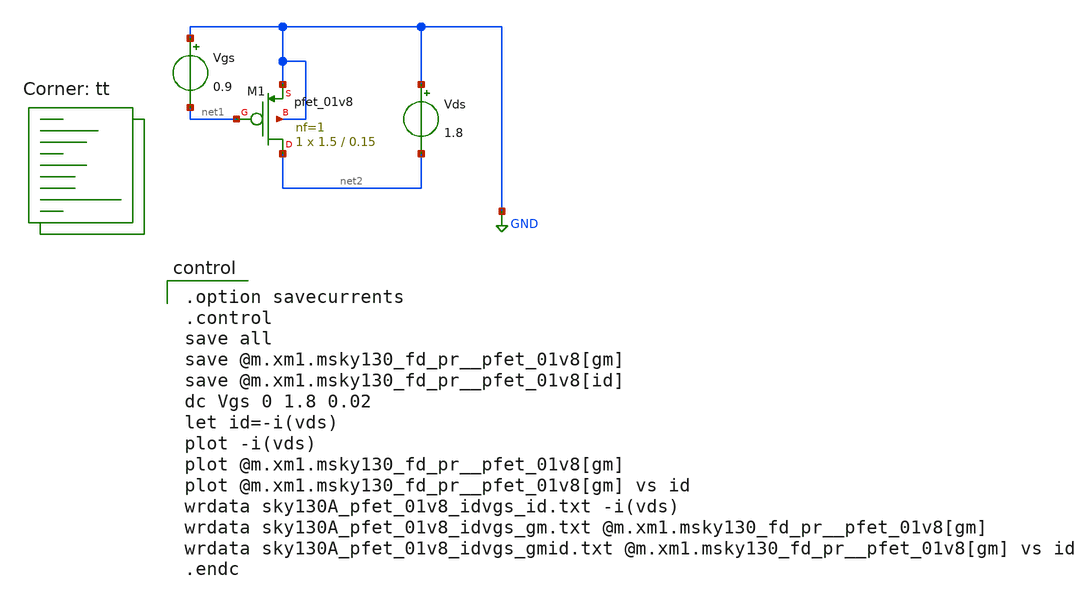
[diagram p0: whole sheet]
** sch_path: xschem/MOSFET/sky130A_pfet_01v8_idvgs.sch
**.subckt sky130A_pfet_01v8_idvgs
Vgs GND net1 0.9
Vds GND net2 1.8
XM1 net2 net1 GND GND sky130_fd_pr__pfet_01v8 L=0.15 W=1.5 nf=1 ad='int((nf+1)/2) * W/nf * 0.29' as='int((nf+2)/2) * W/nf * 0.29'
+ pd='2*int((nf+1)/2) * (W/nf + 0.29)' ps='2*int((nf+2)/2) * (W/nf + 0.29)' nrd='0.29 / W' nrs='0.29 / W'
+ sa=0 sb=0 sd=0 mult=1 m=1
**** begin user architecture code

.option savecurrents
.control
save all
save @m.xm1.msky130_fd_pr__pfet_01v8[gm]
save @m.xm1.msky130_fd_pr__pfet_01v8[id]
dc Vgs 0 1.8 0.02
let id=-i(vds)
plot -i(vds)
plot @m.xm1.msky130_fd_pr__pfet_01v8[gm]
plot @m.xm1.msky130_fd_pr__pfet_01v8[gm] vs id
wrdata sky130A_pfet_01v8_idvgs_id.txt -i(vds)
wrdata sky130A_pfet_01v8_idvgs_gm.txt @m.xm1.msky130_fd_pr__pfet_01v8[gm]
wrdata sky130A_pfet_01v8_idvgs_gmid.txt @m.xm1.msky130_fd_pr__pfet_01v8[gm] vs id
.endc

.lib $::SKYWATER_MODELS/sky130.lib.spice tt
**** end user architecture code
**.ends
.GLOBAL GND
.end
